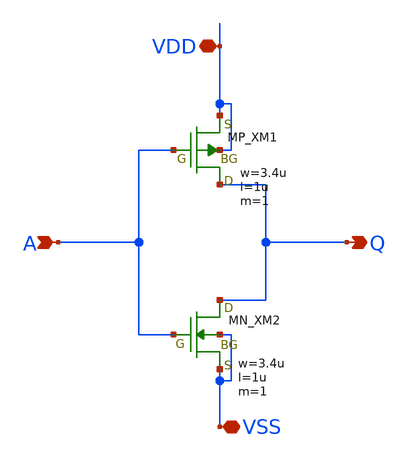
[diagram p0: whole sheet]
** sch_path: schematic/20250924_OSS_Workshop/Qdai/inverter_MUX_02/inv_lihaitao.sch
**.subckt inv_lihaitao A Q VDD VSS
*.ipin A
*.opin Q
*.iopin VDD
*.iopin VSS
XM1 Q A VDD VDD PMOS w=3.4u l=1u as=0 ad=0 ps=0 pd=0 nrd=0 nrs=0 m=1
XM2 Q A VSS VSS NMOS w=3.4u l=1u as=0 ad=0 ps=0 pd=0 nrd=0 nrs=0 m=1
**.ends
.end
